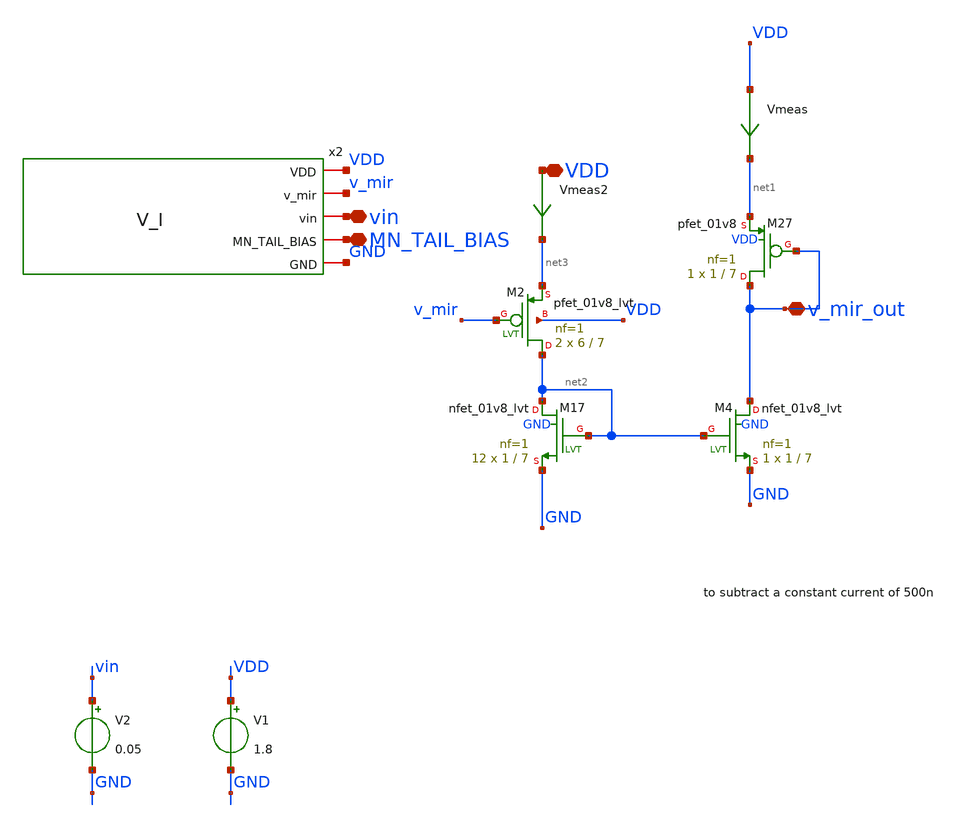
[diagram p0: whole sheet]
** sch_path: xschem/tb/V_I_tb.sch
**.subckt V_I_tb v_mir_out VDD vin MN_TAIL_BIAS
*.iopin v_mir_out
*.iopin VDD
*.iopin vin
*.iopin MN_TAIL_BIAS
V1 VDD GND 1.8
V2 vin GND 0.05
Vmeas VDD net1 0
.save i(vmeas)
XM2 net2 v_mir net3 VDD sky130_fd_pr__pfet_01v8_lvt L=7 W=6 nf=1 ad='int((1 + 1)/2) * 6 / 1 * 0.29' as='int((1 + 2)/2) * 6 / 1 * 0.29'
+ pd='2*int((1 + 1)/2) * (6 / 1 + 0.29)' ps='2*int((1 + 2)/2) * (6 / 1 + 0.29)' nrd='0.29 / 6 ' nrs='0.29 / 6 '
+ sa=0 sb=0 sd=0 mult=2 m=2
XM17 net2 net2 GND GND sky130_fd_pr__nfet_01v8_lvt L=7 W=1 nf=1 ad='int((1 + 1)/2) * 1 / 1 * 0.29' as='int((1 + 2)/2) * 1 / 1 * 0.29'
+ pd='2*int((1 + 1)/2) * (1 / 1 + 0.29)' ps='2*int((1 + 2)/2) * (1 / 1 + 0.29)' nrd='0.29 / 1 ' nrs='0.29 / 1 '
+ sa=0 sb=0 sd=0 mult=12 m=12
XM4 v_mir_out net2 GND GND sky130_fd_pr__nfet_01v8_lvt L=7 W=1 nf=1 ad='int((1 + 1)/2) * 1 / 1 * 0.29'
+ as='int((1 + 2)/2) * 1 / 1 * 0.29' pd='2*int((1 + 1)/2) * (1 / 1 + 0.29)' ps='2*int((1 + 2)/2) * (1 / 1 + 0.29)'
+ nrd='0.29 / 1 ' nrs='0.29 / 1 ' sa=0 sb=0 sd=0 mult=1 m=1
XM27 v_mir_out v_mir_out net1 VDD sky130_fd_pr__pfet_01v8 L=7 W=1 nf=1 ad='int((1 + 1)/2) * 1 / 1 * 0.29'
+ as='int((1 + 2)/2) * 1 / 1 * 0.29' pd='2*int((1 + 1)/2) * (1 / 1 + 0.29)' ps='2*int((1 + 2)/2) * (1 / 1 + 0.29)'
+ nrd='0.29 / 1 ' nrs='0.29 / 1 ' sa=0 sb=0 sd=0 mult=1 m=1
x2 VDD v_mir vin MN_TAIL_BIAS GND V_I
Vmeas2 VDD net3 0
.save i(vmeas2)
**** begin user architecture code

** opencircuitdesign pdks install
.lib /foss/pdks/sky130A/libs.tech/combined/sky130.lib.spice ss
.options temp=27




.options savecurrents
.control

op
dc V2 0 1.8 0.005
write V_I_tb.raw
plot i(vmeas)
.endc


**** end user architecture code
**.ends
.end
